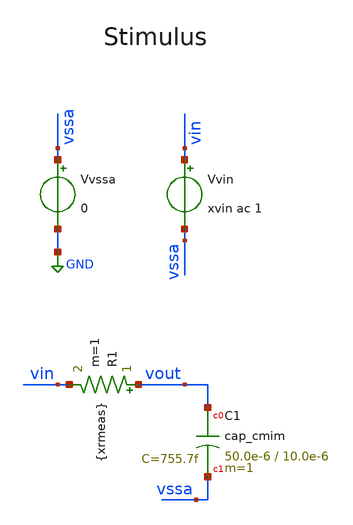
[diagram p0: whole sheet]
** sch_path: tb_cap_ihp/tb_cap_mc_ihp.sch
**.subckt tb_cap_mc_ihp
R1 vout vin {xrmeas} m=1
Vvssa vssa GND 0
Vvin vin vssa xvin ac 1
XC1 vout vssa cap_cmim w=50.0e-6 l=10.0e-6 m=1 mm_ok=1
**** begin user architecture code

** opencircuitdesign pdks install
*.lib /home/slice/pdk/iHP/IHP-Open-PDK/ihp-sg13g2/libs.tech/ngspice/models/cornerMOSlv.lib mos_tt
*.lib /home/slice/pdk/iHP/IHP-Open-PDK/ihp-sg13g2/libs.tech/ngspice/models/cornerMOShv.lib mos_tt
*.lib /home/slice/pdk/iHP/IHP-Open-PDK/ihp-sg13g2/libs.tech/ngspice/models/cornerCAP.lib cap_typ
.lib /home/slice/pdk/iHP/IHP-Open-PDK/ihp-sg13g2/libs.tech/ngspice/models/cornerCAP.lib cap_typ_mismatch


* Parameters
.param xvin = -3.4
.param xrmeas = 1k
.param xCval = 1p
.csparam xvin_var = 'xvin'
.csparam xrmeas_var = 'xrmeas'
.temp 27


  ** must save the below for DCOP analysis to be back annotated onto the schematic
  .option savecurrents

  .include tb_cmeas_ihp.save

  *.save all
  .save v(vin) v(vout)
  .save @n.xm1.nsg13_lv_nmos[ids] @n.xm2.nsg13_hv_nmos[ids] @n.xm3.nsg13_lv_pmos[ids] @n.xm4.nsg13_hv_pmos[ids]

  .control

  let run = 1

  dowhile run <= 100
  reset

  ** 1. AC ANALYSIS **

  ac dec 10 1 1000G

    ** 2. MEASURES **

  let n45_rads = -45*(pi/180)
  echo "$&n45_rads"
  meas AC BW WHEN vp(vout)=n45_rads CROSS=1
  echo "$&BW"
  echo --
  let cmeas = 1/(2*pi*xrmeas_var*BW)
  echo "$&cmeas"
  echo "$&cmeas" >> cap_measures_typ_mc.txt

  remzerovec
  set filetype=binary
  ** first write deletes existing file
  write tb_cap_ihp_mc.raw
  ** set appendwrite appends following writes to existing raw file
  set appendwrite
  let run = run+1

  end

  setplot
quit 0
.endc




**** end user architecture code
**.ends
.GLOBAL GND
.end
